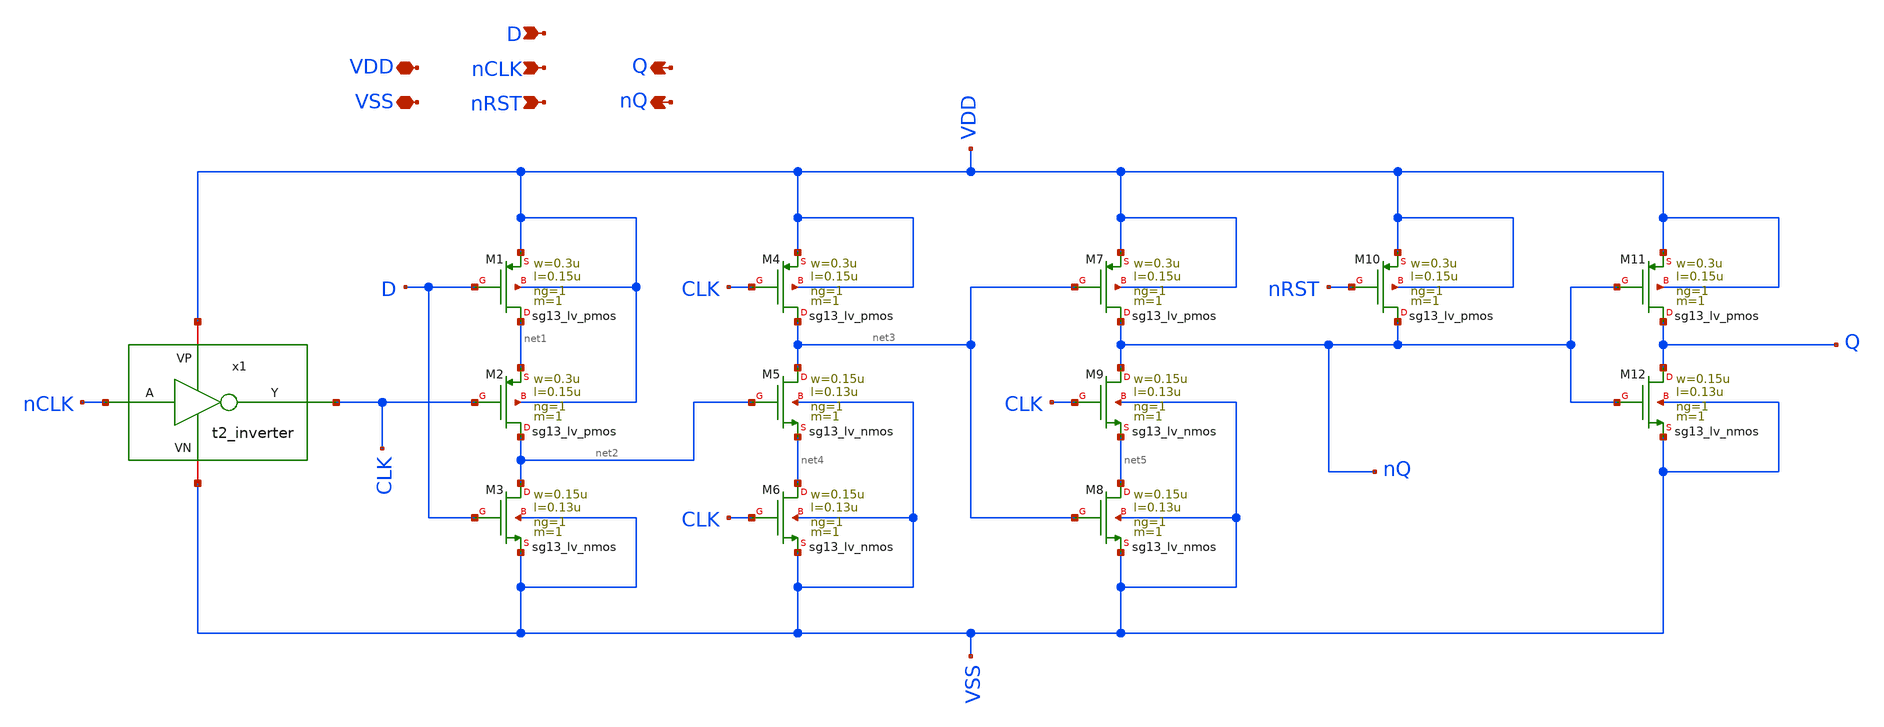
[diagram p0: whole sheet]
** sch_path: Team 2 Design/design_data/xschem/t2_dff_2.sch
**.subckt t2_dff_2 VSS D nRST Q VDD nQ nCLK
*.iopin VSS
*.ipin D
*.ipin nRST
*.opin Q
*.iopin VDD
*.opin nQ
*.ipin nCLK
XM1 net1 D VDD VDD sg13_lv_pmos w=0.3u l=0.15u ng=1 m=1 mm_ok=1
XM2 net2 CLK net1 VDD sg13_lv_pmos w=0.3u l=0.15u ng=1 m=1 mm_ok=1
XM3 net2 D VSS VSS sg13_lv_nmos w=0.15u l=0.13u ng=1 m=1 mm_ok=1
XM4 net3 CLK VDD VDD sg13_lv_pmos w=0.3u l=0.15u ng=1 m=1 mm_ok=1
XM6 net4 CLK VSS VSS sg13_lv_nmos w=0.15u l=0.13u ng=1 m=1 mm_ok=1
XM5 net3 net2 net4 VSS sg13_lv_nmos w=0.15u l=0.13u ng=1 m=1 mm_ok=1
XM7 nQ net3 VDD VDD sg13_lv_pmos w=0.3u l=0.15u ng=1 m=1 mm_ok=1
XM8 net5 net3 VSS VSS sg13_lv_nmos w=0.15u l=0.13u ng=1 m=1 mm_ok=1
XM9 nQ CLK net5 VSS sg13_lv_nmos w=0.15u l=0.13u ng=1 m=1 mm_ok=1
XM10 nQ nRST VDD VDD sg13_lv_pmos w=0.3u l=0.15u ng=1 m=1 mm_ok=1
XM11 Q nQ VDD VDD sg13_lv_pmos w=0.3u l=0.15u ng=1 m=1 mm_ok=1
XM12 Q nQ VSS VSS sg13_lv_nmos w=0.15u l=0.13u ng=1 m=1 mm_ok=1
x1 VDD nCLK CLK VSS t2_inverter
**.ends

* expanding   symbol:  t2_inverter.sym # of pins=4
** sym_path: Team 2 Design/design_data/xschem/t2_inverter.sym
** sch_path: Team 2 Design/design_data/xschem/t2_inverter.sch
.subckt t2_inverter VP A Y VN
*.iopin VP
*.iopin VN
*.ipin A
*.opin Y
XM2 Y A VP VP sg13_lv_pmos w=0.3u l=0.13u ng=1 m=1 mm_ok=1
XM1 Y A VN VN sg13_lv_nmos w=0.15u l=0.13u ng=1 m=1 mm_ok=1
.ends

.end
